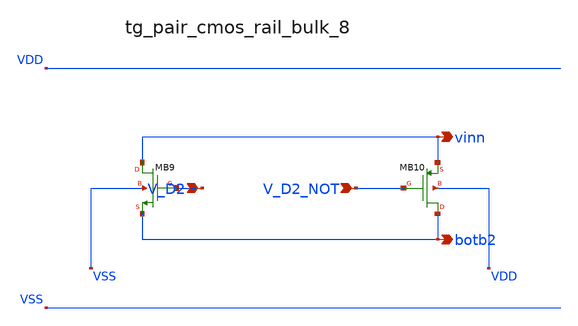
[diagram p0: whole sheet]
** sch_path: analog-db/raw/ia_005_hsu_pga_ideal/hier/blocks/tg_pair_cmos_rail_bulk_8.sch
**.subckt tg_pair_cmos_rail_bulk_8 V_D2 V_D2_NOT vinn botb2
*.ipin V_D2
*.ipin V_D2_NOT
*.opin vinn
*.opin botb2
XMB10 botb2 V_D2_NOT vinn VDD sg13_lv_pmos w=x_dut_xmb10_w l=x_dut_xmb10_l ng=1 m=x_dut_xmb10_m
XMB9 vinn V_D2 botb2 VSS sg13_lv_nmos w=x_dut_xmb9_w l=x_dut_xmb9_l ng=1 m=x_dut_xmb9_m
**.ends
.end
